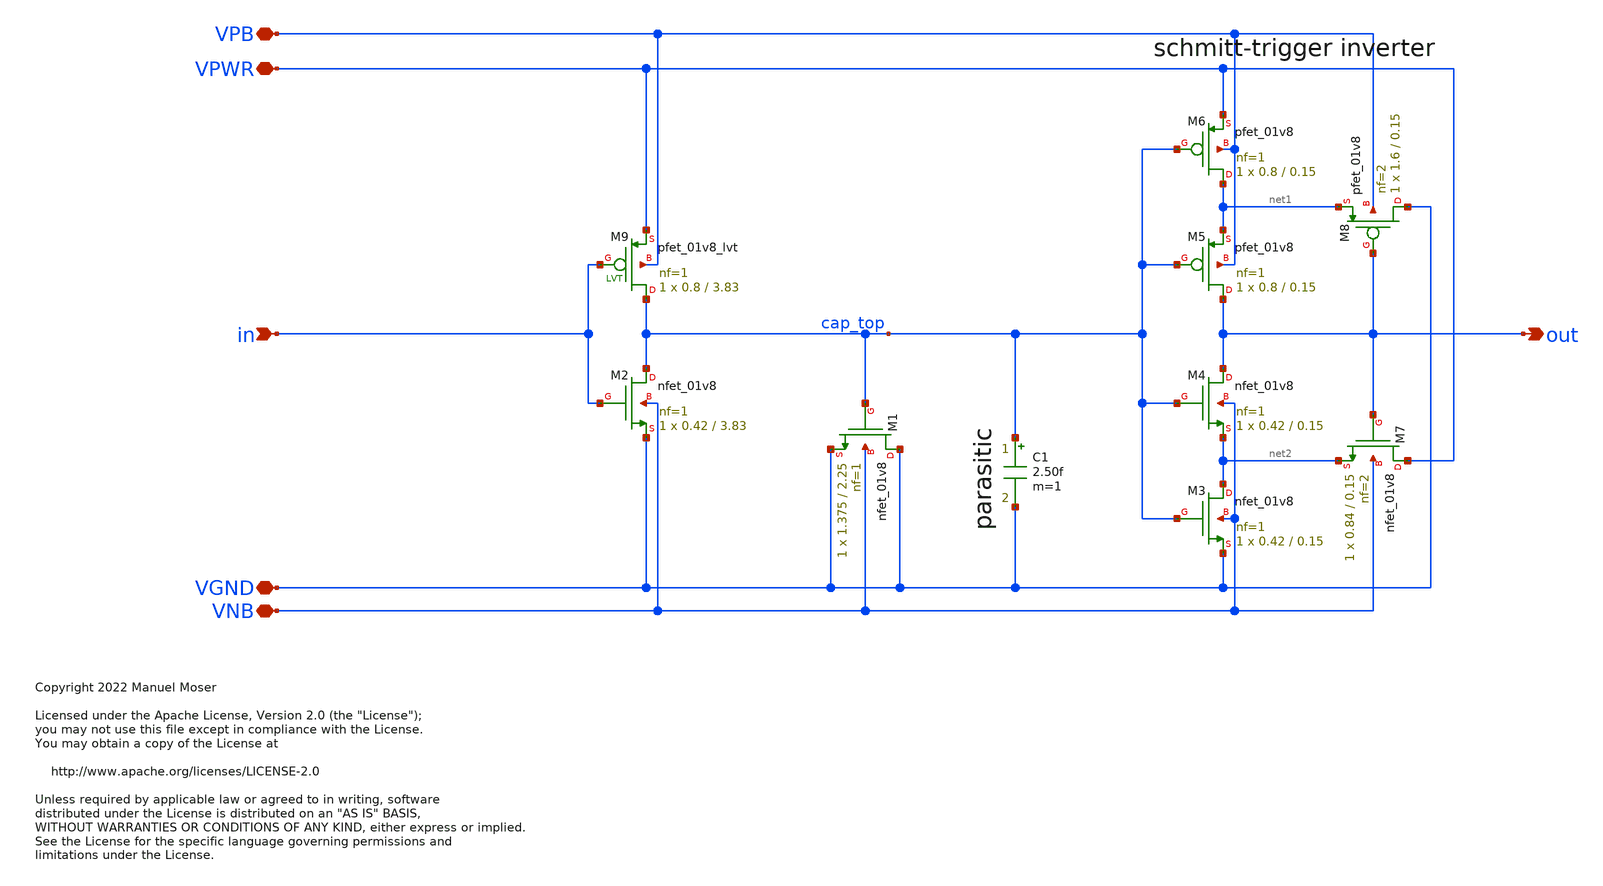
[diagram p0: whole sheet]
** sch_path: xschem/sky130_mm_sc_hd_dlyPoly6ns/sky130_mm_sc_hd_dlyPoly6ns.sch
* Copyright 2022 Manuel Moser
* Licensed under the Apache License, Version 2.0 (the "License");
**.subckt sky130_mm_sc_hd_dlyPoly6ns VPWR VGND in out VPB VNB
*.iopin VPWR
*.iopin VGND
*.ipin in
*.opin out
*.iopin VPB
*.iopin VNB
XM2 cap_top in VGND VNB sky130_fd_pr__nfet_01v8 L=3.83 W=0.42 nf=1 ad='int((nf+1)/2) * W/nf * 0.29' as='int((nf+2)/2) * W/nf * 0.29'
+ pd='2*int((nf+1)/2) * (W/nf + 0.29)' ps='2*int((nf+2)/2) * (W/nf + 0.29)' nrd='0.29 / W' nrs='0.29 / W'
+ sa=0 sb=0 sd=0 mult=1 m=1
XM3 net2 cap_top VGND VNB sky130_fd_pr__nfet_01v8 L=0.15 W=0.42 nf=1 ad='int((nf+1)/2) * W/nf * 0.29'
+ as='int((nf+2)/2) * W/nf * 0.29' pd='2*int((nf+1)/2) * (W/nf + 0.29)' ps='2*int((nf+2)/2) * (W/nf + 0.29)'
+ nrd='0.29 / W' nrs='0.29 / W' sa=0 sb=0 sd=0 mult=1 m=1
XM4 out cap_top net2 VNB sky130_fd_pr__nfet_01v8 L=0.15 W=0.42 nf=1 ad='int((nf+1)/2) * W/nf * 0.29'
+ as='int((nf+2)/2) * W/nf * 0.29' pd='2*int((nf+1)/2) * (W/nf + 0.29)' ps='2*int((nf+2)/2) * (W/nf + 0.29)'
+ nrd='0.29 / W' nrs='0.29 / W' sa=0 sb=0 sd=0 mult=1 m=1
XM5 out cap_top net1 VPB sky130_fd_pr__pfet_01v8 L=0.15 W=0.8 nf=1 ad='int((nf+1)/2) * W/nf * 0.29' as='int((nf+2)/2) * W/nf * 0.29'
+ pd='2*int((nf+1)/2) * (W/nf + 0.29)' ps='2*int((nf+2)/2) * (W/nf + 0.29)' nrd='0.29 / W' nrs='0.29 / W'
+ sa=0 sb=0 sd=0 mult=1 m=1
XM6 net1 cap_top VPWR VPB sky130_fd_pr__pfet_01v8 L=0.15 W=0.8 nf=1 ad='int((nf+1)/2) * W/nf * 0.29'
+ as='int((nf+2)/2) * W/nf * 0.29' pd='2*int((nf+1)/2) * (W/nf + 0.29)' ps='2*int((nf+2)/2) * (W/nf + 0.29)'
+ nrd='0.29 / W' nrs='0.29 / W' sa=0 sb=0 sd=0 mult=1 m=1
XM7 VPWR out net2 VNB sky130_fd_pr__nfet_01v8 L=0.15 W=0.84 nf=2 ad='int((nf+1)/2) * W/nf * 0.29' as='int((nf+2)/2) * W/nf * 0.29'
+ pd='2*int((nf+1)/2) * (W/nf + 0.29)' ps='2*int((nf+2)/2) * (W/nf + 0.29)' nrd='0.29 / W' nrs='0.29 / W'
+ sa=0 sb=0 sd=0 mult=1 m=1
XM8 VGND out net1 VPB sky130_fd_pr__pfet_01v8 L=0.15 W=1.6 nf=2 ad='int((nf+1)/2) * W/nf * 0.29' as='int((nf+2)/2) * W/nf * 0.29'
+ pd='2*int((nf+1)/2) * (W/nf + 0.29)' ps='2*int((nf+2)/2) * (W/nf + 0.29)' nrd='0.29 / W' nrs='0.29 / W'
+ sa=0 sb=0 sd=0 mult=1 m=1
XM9 cap_top in VPWR VPB sky130_fd_pr__pfet_01v8_lvt L=3.83 W=0.8 nf=1 ad='int((nf+1)/2) * W/nf * 0.29'
+ as='int((nf+2)/2) * W/nf * 0.29' pd='2*int((nf+1)/2) * (W/nf + 0.29)' ps='2*int((nf+2)/2) * (W/nf + 0.29)'
+ nrd='0.29 / W' nrs='0.29 / W' sa=0 sb=0 sd=0 mult=1 m=1
XM1 VGND cap_top VGND VNB sky130_fd_pr__nfet_01v8 L=2.25 W=1.375 nf=1 ad='int((nf+1)/2) * W/nf * 0.29'
+ as='int((nf+2)/2) * W/nf * 0.29' pd='2*int((nf+1)/2) * (W/nf + 0.29)' ps='2*int((nf+2)/2) * (W/nf + 0.29)'
+ nrd='0.29 / W' nrs='0.29 / W' sa=0 sb=0 sd=0 mult=1 m=1
C1 cap_top VGND 2.50f m=1
**.ends
.end
